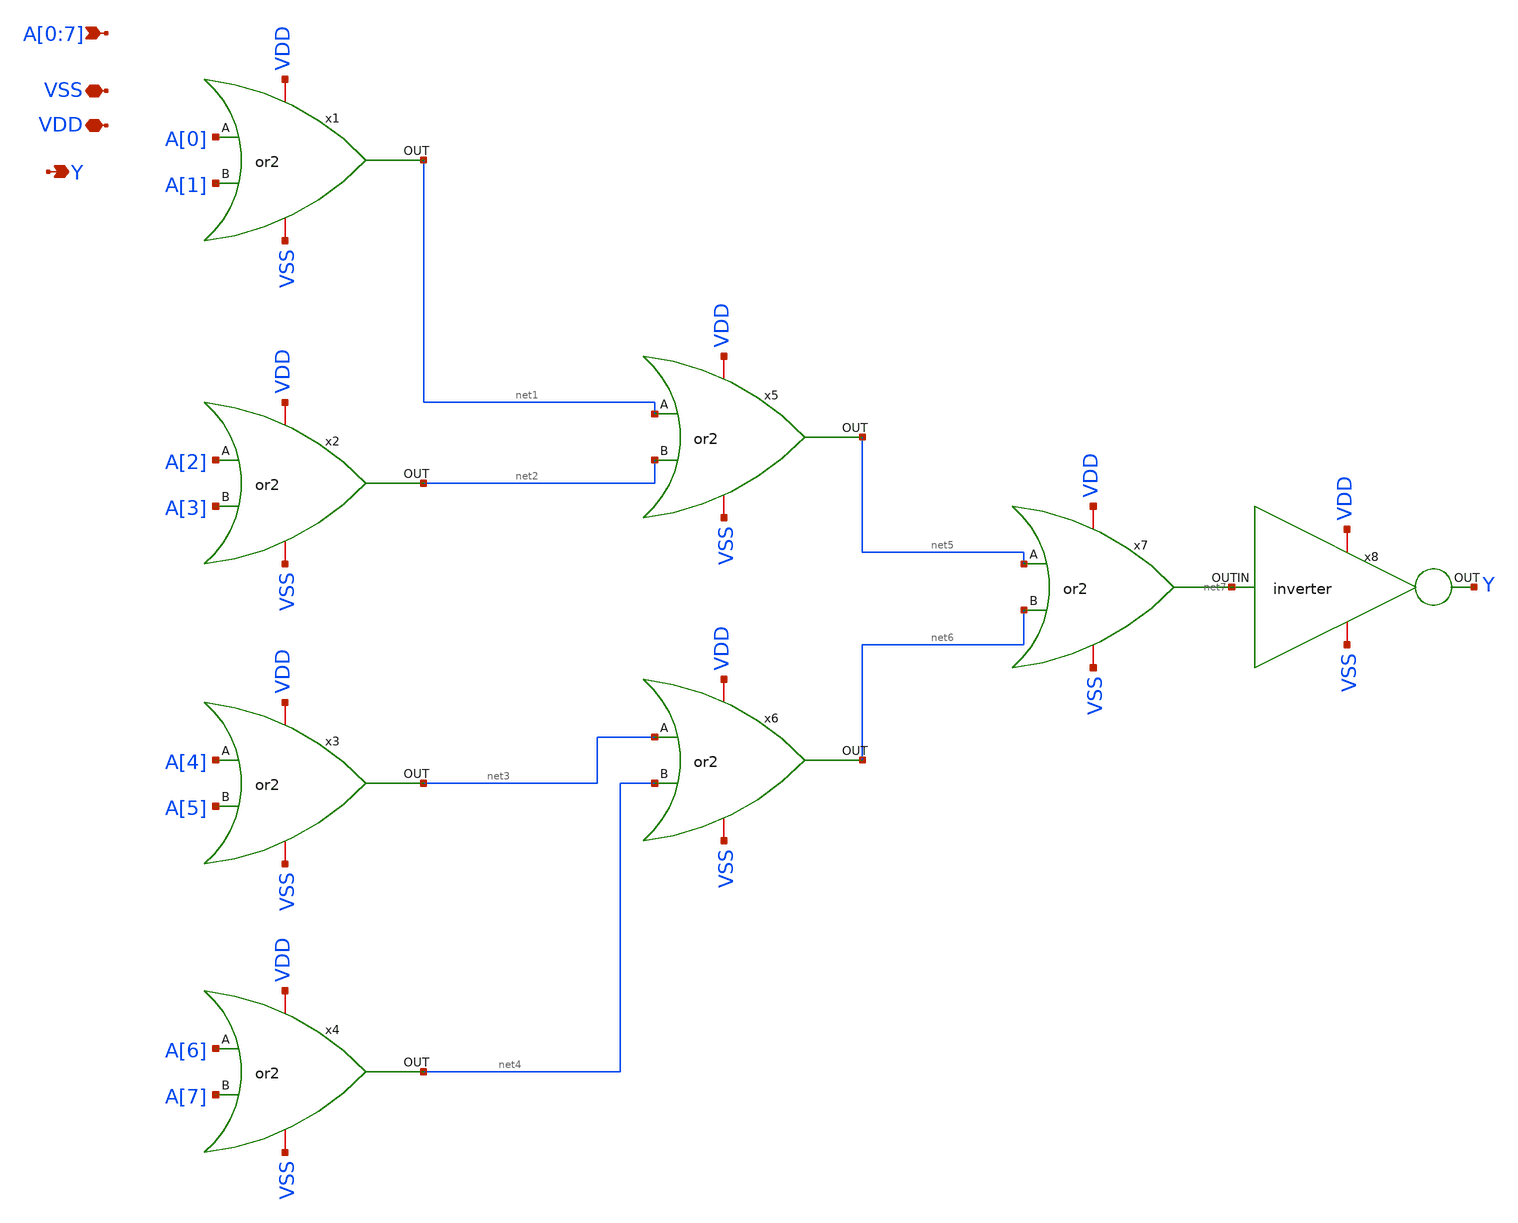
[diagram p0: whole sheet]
** sch_path: design/NOR8/xschem/nor8.sch
**.subckt nor8 A[0],A[1],A[2],A[3],A[4],A[5],A[6],A[7] VDD VSS Y
*.ipin A[0],A[1],A[2],A[3],A[4],A[5],A[6],A[7]
*.iopin VDD
*.iopin VSS
*.opin Y
x1 A[0] A[1] VSS VDD net1 or2
x2 A[2] A[3] VSS VDD net2 or2
x3 A[4] A[5] VSS VDD net3 or2
x4 A[6] A[7] VSS VDD net4 or2
x5 net1 net2 VSS VDD net5 or2
x6 net3 net4 VSS VDD net6 or2
x7 net5 net6 VSS VDD net7 or2
x8 VDD Y net7 VSS inverter
**.ends

* expanding   symbol:  or2.sym # of pins=5
** sym_path: design/8_BIT_OR/xschem/or2.sym
** sch_path: design/8_BIT_OR/xschem/or2.sch
.subckt or2 A B VSS VDD OUT
*.ipin A
*.ipin B
*.iopin VSS
*.iopin VDD
*.opin OUT
XM3 net1 A net2 VDD sky130_fd_pr__pfet_01v8 L=0.15 W=6.4 nf=1 ad='int((nf+1)/2) * W/nf * 0.29' as='int((nf+2)/2) * W/nf * 0.29'
+ pd='2*int((nf+1)/2) * (W/nf + 0.29)' ps='2*int((nf+2)/2) * (W/nf + 0.29)' nrd='0.29 / W' nrs='0.29 / W'
+ sa=0 sb=0 sd=0 mult=1 m=1
XM4 net2 B VDD VDD sky130_fd_pr__pfet_01v8 L=0.15 W=6.4 nf=1 ad='int((nf+1)/2) * W/nf * 0.29' as='int((nf+2)/2) * W/nf * 0.29'
+ pd='2*int((nf+1)/2) * (W/nf + 0.29)' ps='2*int((nf+2)/2) * (W/nf + 0.29)' nrd='0.29 / W' nrs='0.29 / W'
+ sa=0 sb=0 sd=0 mult=1 m=1
XM1 net1 A VSS VSS sky130_fd_pr__nfet_01v8 L=0.15 W=1 nf=1 ad='int((nf+1)/2) * W/nf * 0.29' as='int((nf+2)/2) * W/nf * 0.29'
+ pd='2*int((nf+1)/2) * (W/nf + 0.29)' ps='2*int((nf+2)/2) * (W/nf + 0.29)' nrd='0.29 / W' nrs='0.29 / W'
+ sa=0 sb=0 sd=0 mult=1 m=1
XM2 net1 B VSS VSS sky130_fd_pr__nfet_01v8 L=0.15 W=1 nf=1 ad='int((nf+1)/2) * W/nf * 0.29' as='int((nf+2)/2) * W/nf * 0.29'
+ pd='2*int((nf+1)/2) * (W/nf + 0.29)' ps='2*int((nf+2)/2) * (W/nf + 0.29)' nrd='0.29 / W' nrs='0.29 / W'
+ sa=0 sb=0 sd=0 mult=1 m=1
XM5 OUT net1 VDD VDD sky130_fd_pr__pfet_01v8 L=0.15 W=6.4 nf=1 ad='int((nf+1)/2) * W/nf * 0.29' as='int((nf+2)/2) * W/nf * 0.29'
+ pd='2*int((nf+1)/2) * (W/nf + 0.29)' ps='2*int((nf+2)/2) * (W/nf + 0.29)' nrd='0.29 / W' nrs='0.29 / W'
+ sa=0 sb=0 sd=0 mult=1 m=1
XM6 OUT net1 VSS VSS sky130_fd_pr__nfet_01v8 L=0.15 W=1 nf=1 ad='int((nf+1)/2) * W/nf * 0.29' as='int((nf+2)/2) * W/nf * 0.29'
+ pd='2*int((nf+1)/2) * (W/nf + 0.29)' ps='2*int((nf+2)/2) * (W/nf + 0.29)' nrd='0.29 / W' nrs='0.29 / W'
+ sa=0 sb=0 sd=0 mult=1 m=1
.ends


* expanding   symbol:  inverter.sym # of pins=4
** sym_path: design/ALU/inverter.sym
** sch_path: design/ALU/inverter.sch
.subckt inverter VDD OUT IN VSS
*.ipin IN
*.iopin VDD
*.opin OUT
*.iopin VSS
XM2 OUT IN VDD VDD sky130_fd_pr__pfet_01v8 L=0.15 W=0.9 nf=1 ad='int((nf+1)/2) * W/nf * 0.29' as='int((nf+2)/2) * W/nf * 0.29'
+ pd='2*int((nf+1)/2) * (W/nf + 0.29)' ps='2*int((nf+2)/2) * (W/nf + 0.29)' nrd='0.29 / W' nrs='0.29 / W'
+ sa=0 sb=0 sd=0 mult=1 m=1
XM1 OUT IN VSS VSS sky130_fd_pr__nfet_01v8 L=0.15 W=0.42 nf=1 ad='int((1 + 1)/2) * 0.42 / 1 * 0.29' as='int((1 + 2)/2) * 0.42 / 1 * 0.29'
+ pd='2*int((1 + 1)/2) * (0.42 / 1 + 0.29)' ps='2*int((1 + 2)/2) * (0.42 / 1 + 0.29)' nrd='0.29 / 0.42 '
+ nrs='0.29 / 0.42 ' sa=0 sb=0 sd=0 mult=1 m=1
.ends

.end
